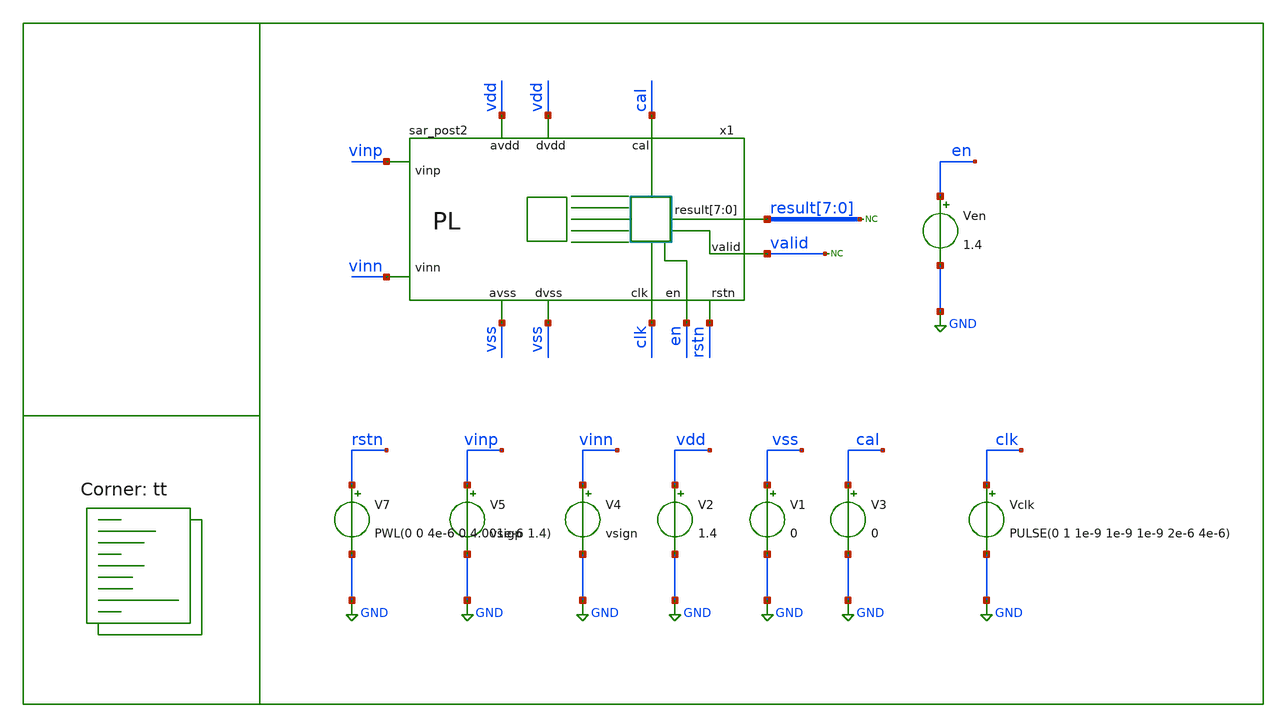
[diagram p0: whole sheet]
** sch_path: new_layout/simulations/tb_sar_analog.sch

.include /home/alex/Desktop/EDA/SAR_IPN/new_layout/simulations/spice/sar_analog.spice
.include /home/alex/Desktop/EDA/SAR_IPN/new_layout/simulations/spice/cmos_cells_digital.sp
.include /home/alex/Desktop/EDA/SAR_IPN/new_layout/simulations/spice/sar_logic.sp
.include $::SKYWATER_STDCELLS/sky130_fd_sc_hd.spice


.lib $::SKYWATER_MODELS/sky130.lib.spice tt
**.subckt tb_sar_analog
V1 vss GND 0
V2 vdd GND 1.4
V4 vinn GND vsign
V5 vinp GND vsigp
Vclk clk GND PULSE(0 1 1e-9 1e-9 1e-9 2e-6 4e-6)
Ven en GND 1.4
* noconn valid
V3 cal GND 0
* noconn result[7:0]
V7 rstn GND PWL(0 0 4e-6 0 4.001e-6 1.4)
x1 vdd vdd vss result[7] result[6] result[5] result[4] result[3] result[2] result[1] result[0] vinn
+ vss clk vinp en valid cal rstn sar_post2
**.ends

* expanding   symbol:  /home/alex/Desktop/EDA/SAR_IPN/new_layout/simulations/symbols/sar_post2.sym #
*+ of pins=12
** sym_path: new_layout/simulations/symbols/sar_post2.sym
** sch_path: new_layout/simulations/symbols/sar_post2.sch
.subckt sar_post2 avdd dvdd dvss result[7] result[6] result[5] result[4] result[3] result[2]
+ result[1] result[0] vinn avss clk vinp en valid cal rstn
*.iopin avss
*.iopin avdd
*.iopin dvss
*.iopin dvdd
*.ipin vinp
*.ipin vinn
*.opin result[7],result[6],result[5],result[4],result[3],result[2],result[1],result[0]
*.ipin clk
*.ipin en
*.opin valid
*.ipin cal
*.ipin rstn
* noconn comp
* noconn result[7:0]
* noconn valid
* noconn clkc
* noconn clk
* noconn en
* noconn cal
* noconn rstn
**** begin user architecture code



.model adc_buff adc_bridge(in_low = 0.2 in_high=0.8)
.model dac_buff dac_bridge(out_high = 1.2)

Aad [clk rstn en comp cal] [dclk drstn den dcomp dcal] adc_buff
Ada [dctlp0 dctlp1 dctlp2 dctlp3 dctlp4 dctlp5 dctlp6 dctlp7 dctln0 dctln1 dctln2 dctln3 dctln4
+ dctln5 dctln6 dctln7 dres0 dres1 dres2 dres3 dres4 dres5 dres6 dres7 dsamp dclkc] [ctlp_0_ ctlp_1_ ctlp_2_
+ ctlp_3_ ctlp_4_ ctlp_5_ ctlp_6_ ctlp_7_ ctln_0_ ctln_1_ ctln_2_ ctln_3_ ctln_4_ ctln_5_ ctln_6_ ctln_7_
+ res0 res1 res2 res3 res4 res5 res6 res7 sample clkc] dac_buff
Ada2 [dtrim4 dtrim3 dtrim2 dtrim1 dtrim0 dtrimb4 dtrimb3 dtrimb2 dtrimb1 dtrimb0] [trim_4_ trim_3_
+ trim_2_ trim_1_ trim_0_ trimb_4_ trimb_3_ trimb_2_ trimb_1_ trimb_0_ ] dac_buff
Xuut dclk drstn den dcomp dcal dvalid dres0 dres1 dres2 dres3 dres4 dres5 dres6 dres7 dsamp dctlp0
+ dctlp1 dctlp2 dctlp3 dctlp4 dctlp5 dctlp6 dctlp7 dctln0 dctln1 dctln2 dctln3 dctln4 dctln5 dctln6 dctln7
+ dtrim0 dtrim1 dtrim2 dtrim3 dtrim4 dtrimb0 dtrimb1 dtrimb2 dtrimb3 dtrimb4 dclkc sar_logic


**** end user architecture code
* noconn dvdd
* noconn dvss
x1 ctlp[7] ctlp[6] ctlp[5] ctlp[4] ctlp[3] ctlp[2] ctlp[1] ctlp[0] ctln[7] ctln[6] ctln[5] ctln[4]
+ ctln[3] ctln[2] ctln[1] ctln[0] trim[4] trim[3] trim[2] trim[1] trim[0] trimb[4] trimb[3] trimb[2] trimb[1]
+ trimb[0] vinp vinn sample comp clkc avdd avss sar_analog
* noconn trim[4:0]
* noconn trimb[4:0]
* noconn sample
* noconn ctlp[7:0]
* noconn ctln[7:0]
.ends

.GLOBAL GND
**** begin user architecture code

.options method trap
*.options method gear
.options gmin 1e-15
.options abstol 1e-15
.options reltol 0.0001
.options vntol 0.1e-6
.options warn 1

.param MC_SWITCH=0
.param vin=0.2
.param vcm=0.7
.param vsigp={vcm + vin/2}
.param vsign={vcm - vin/2}

.tran 100e-9 48e-6
.save all
.control

run
write tb_sar_analog.raw
meas tran d0 find v(xsar.res0) at=47e-6
meas tran d1 find v(xsar.res1) at=47e-6
meas tran d2 find v(xsar.res2) at=47e-6
meas tran d3 find v(xsar.res3) at=47e-6
meas tran d4 find v(xsar.res4) at=47e-6
meas tran d5 find v(xsar.res5) at=47e-6
meas tran d6 find v(xsar.res6) at=47e-6
meas tran d7 find v(xsar.res7) at=47e-6

* meas tran d0 find v(xsar.result0) at=47e-6
* meas tran d1 find v(xsar.result1) at=47e-6
* meas tran d2 find v(xsar.result2) at=47e-6
* meas tran d3 find v(xsar.result3) at=47e-6
* meas tran d4 find v(xsar.result4) at=47e-6
* meas tran d5 find v(xsar.result5) at=47e-6
* meas tran d6 find v(xsar.result6) at=47e-6
* meas tran d7 find v(xsar.result7) at=47e-6

meas tran vpmax max xsar.vp
meas tran vpmin min xsar.vp
meas tran vpend find v(xsar.vp) at=39e-6

meas tran vnmax max xsar.vn
meas tran vnmin min xsar.vn
meas tran vnend find v(xsar.vn) at=39e-6

print d0
print d1
print d2
print d3
print d4
print d5
print d6
print d7

print vpmax
print vpmin

print vnmax
print vnmin

print vpend
print vnend

.endc


**** end user architecture code
.end
